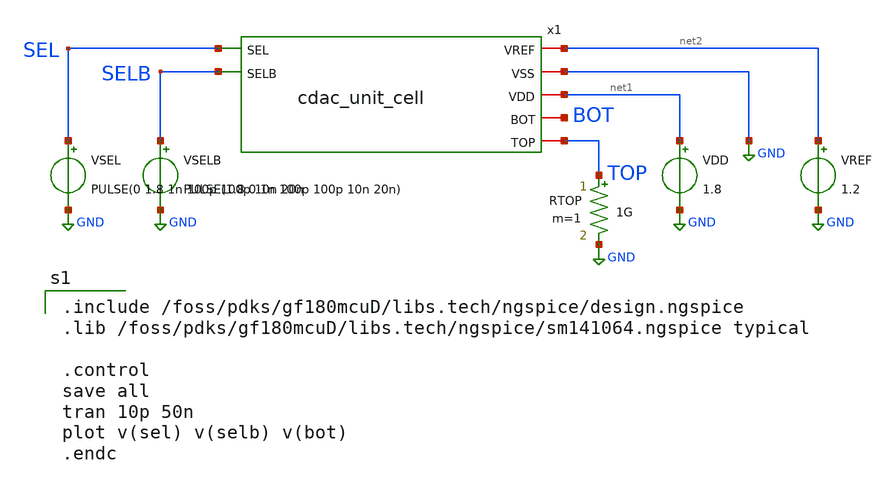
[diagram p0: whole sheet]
** sch_path: designs/libs/tb_matchmaker/tb_cdac_unit_cell/tb_cdac_unit_cell.sch
**.subckt tb_cdac_unit_cell
RTOP TOP GND 1G m=1
VDD net1 GND 1.8
VREF net2 GND 1.2
VSELB SELB GND PULSE(1.8 0 1n 100p 100p 10n 20n)
VSEL SEL GND PULSE(0 1.8 1n 100p 100p 10n 20n
x1 SEL net2 GND SELB net1 BOT TOP cdac_unit_cell
**** begin user architecture code

.include /foss/pdks/gf180mcuD/libs.tech/ngspice/design.ngspice
.lib /foss/pdks/gf180mcuD/libs.tech/ngspice/sm141064.ngspice typical

.control
save all
tran 10p 50n
plot v(sel) v(selb) v(bot)
.endc

**** end user architecture code
**.ends
.GLOBAL GND
.end
